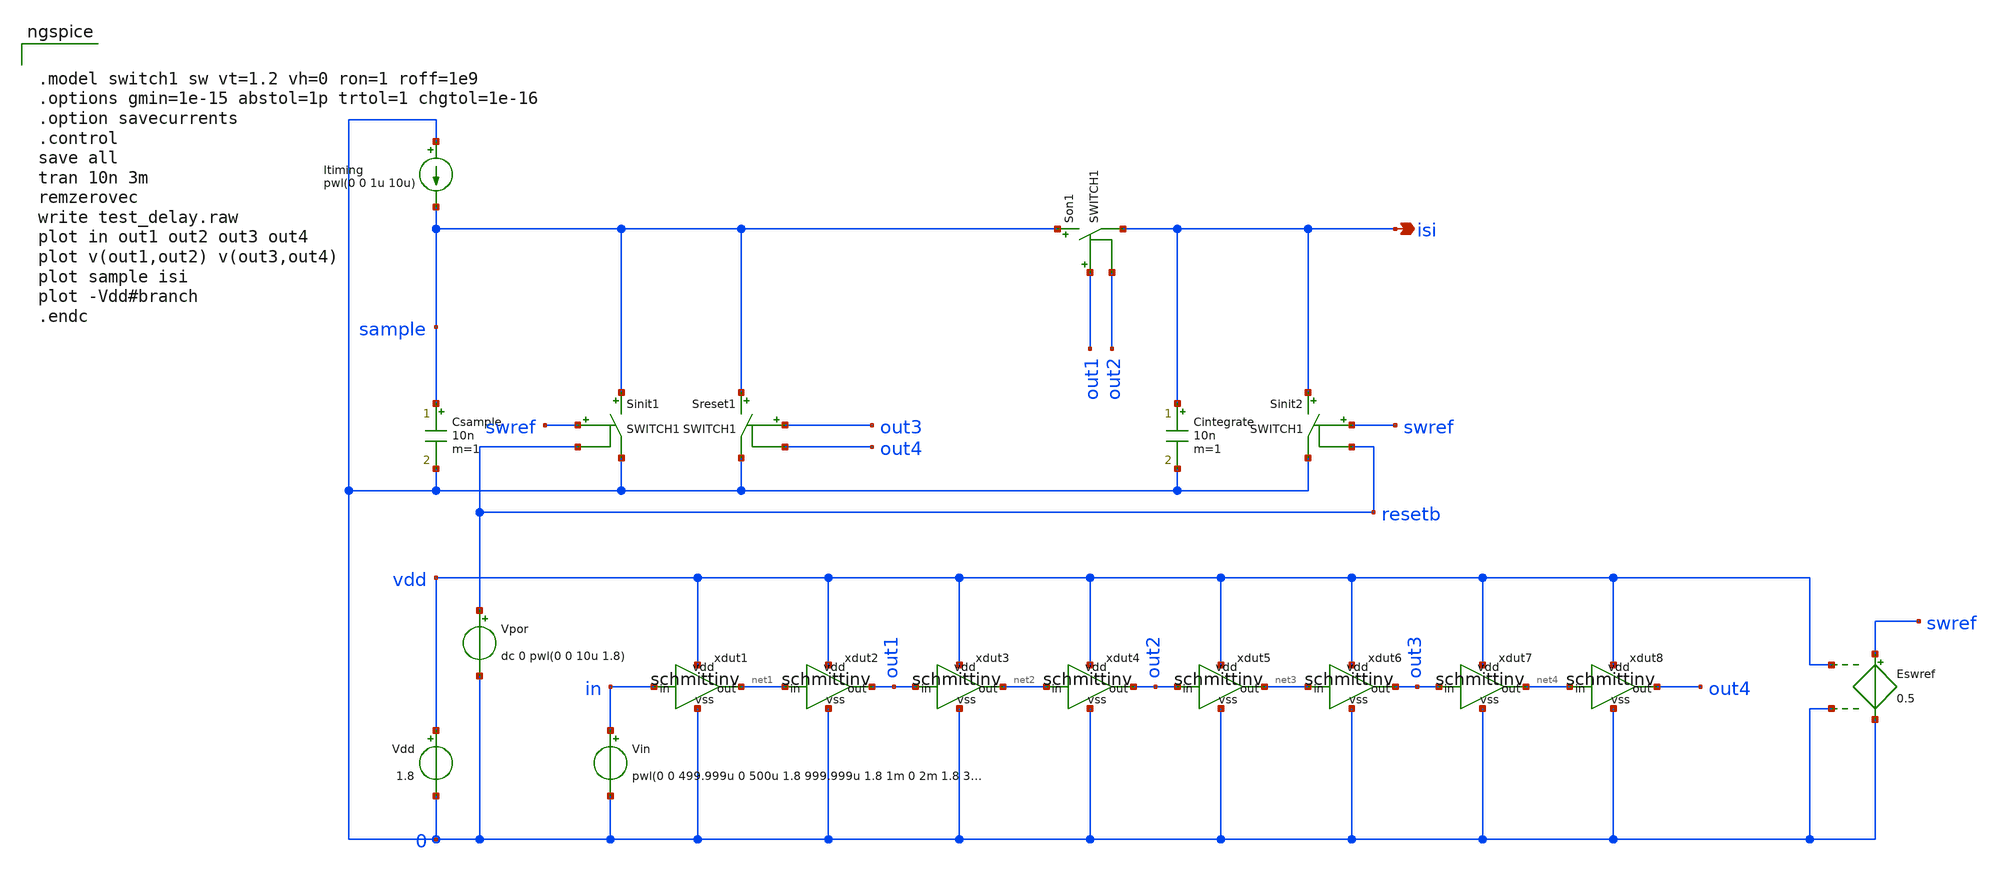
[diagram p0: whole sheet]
** sch_path: xschem/test_delay.sch
* Copyright 2020 Stefan Frederik Schippers
* Licensed under the Apache License, Version 2.0 (the "License");
* you may not use this file except in compliance with the License.
* You may obtain a copy of the License at
* https://www.apache.org/licenses/LICENSE-2.0
* Unless required by applicable law or agreed to in writing, software
* distributed under the License is distributed on an "AS IS" BASIS,
* WITHOUT WARRANTIES OR CONDITIONS OF ANY KIND, either express or implied.
* See the License for the specific language governing permissions and
* limitations under the License.
**.subckt test_delay isi
*.opin isi
Vdd vdd 0 1.8
xdut1 vdd in net1 0 schmittinv
Vin in 0 pwl(0 0 499.999u 0 500u 1.8 999.999u 1.8 1m 0 2m 1.8 3m 0)
xdut2 vdd net1 out1 0 schmittinv
xdut3 vdd out1 net2 0 schmittinv
xdut4 vdd net2 out2 0 schmittinv
Csample sample 0 10n m=1
Itiming 0 sample pwl(0 0 1u 10u)
Cintegrate isi 0 10n m=1
Sreset1 sample 0 out3 out4 SWITCH1
Eswref swref 0 vdd 0 0.5
Son1 sample isi out1 out2 SWITCH1
Sinit1 sample 0 swref resetb SWITCH1
Sinit2 isi 0 swref resetb SWITCH1
Vpor resetb 0 dc 0 pwl(0 0 10u 1.8)
xdut5 vdd out2 net3 0 schmittinv
xdut6 vdd net3 out3 0 schmittinv
xdut7 vdd out3 net4 0 schmittinv
xdut8 vdd net4 out4 0 schmittinv
**** begin user architecture code


.model switch1 sw vt=1.2 vh=0 ron=1 roff=1e9
.options gmin=1e-15 abstol=1p trtol=1 chgtol=1e-16
.option savecurrents
.control
save all
tran 10n 3m
remzerovec
write test_delay.raw
plot in out1 out2 out3 out4
plot v(out1,out2) v(out3,out4)
plot sample isi
plot -Vdd#branch
.endc


 .lib $::SKYWATER_MODELS/sky130.lib.spice tt

.param mc_mm_switch=0
.param mc_pr_switch=1


**** end user architecture code
**.ends

* expanding   symbol:  schmittinv.sym # of pins=4
** sym_path: schmittinv.sym
** sch_path: schmittinv.sch
.subckt schmittinv vdd in out vss
*.iopin vdd
*.iopin vss
*.ipin in
*.opin out
XM1 dn in vss vss sky130_fd_pr__nfet_01v8 L=8 W=0.5 nf=1 ad='int((1 + 1)/2) * 0.5 / 1 * 0.29' as='int((1 + 2)/2) * 0.5 / 1 * 0.29'
+ pd='2*int((1 + 1)/2) * (0.5 / 1 + 0.29)' ps='2*int((1 + 2)/2) * (0.5 / 1 + 0.29)' nrd='0.29 / 0.5 ' nrs='0.29 / 0.5 '
+ sa=0 sb=0 sd=0 mult=1 m=1
XM5 dp in vdd vdd sky130_fd_pr__pfet_01v8 L=2 W=0.5 nf=1 ad='int((nf+1)/2) * W/nf * 0.29' as='int((nf+2)/2) * W/nf * 0.29'
+ pd='2*int((nf+1)/2) * (W/nf + 0.29)' ps='2*int((nf+2)/2) * (W/nf + 0.29)' nrd='0.29 / W' nrs='0.29 / W'
+ sa=0 sb=0 sd=0 mult=1 m=1
XM3 vdd out dsn vss sky130_fd_pr__nfet_01v8 L=12 W=0.5 nf=1 ad='int((1 + 1)/2) * 0.5 / 1 * 0.29' as='int((1 + 2)/2) * 0.5 / 1 * 0.29'
+ pd='2*int((1 + 1)/2) * (0.5 / 1 + 0.29)' ps='2*int((1 + 2)/2) * (0.5 / 1 + 0.29)' nrd='0.29 / 0.5 ' nrs='0.29 / 0.5 '
+ sa=0 sb=0 sd=0 mult=1 m=1
XM6 vss out dp vdd sky130_fd_pr__pfet_01v8 L=4 W=0.5 nf=1 ad='int((nf+1)/2) * W/nf * 0.29' as='int((nf+2)/2) * W/nf * 0.29'
+ pd='2*int((nf+1)/2) * (W/nf + 0.29)' ps='2*int((nf+2)/2) * (W/nf + 0.29)' nrd='0.29 / W' nrs='0.29 / W'
+ sa=0 sb=0 sd=0 mult=1 m=1
XM4 out in dp vdd sky130_fd_pr__pfet_01v8 L=2 W=0.5 nf=1 ad='int((nf+1)/2) * W/nf * 0.29' as='int((nf+2)/2) * W/nf * 0.29'
+ pd='2*int((nf+1)/2) * (W/nf + 0.29)' ps='2*int((nf+2)/2) * (W/nf + 0.29)' nrd='0.29 / W' nrs='0.29 / W'
+ sa=0 sb=0 sd=0 mult=1 m=1
XM2 out in dn vss sky130_fd_pr__nfet_01v8 L=8 W=0.5 nf=1 ad='int((1 + 1)/2) * 0.5 / 1 * 0.29' as='int((1 + 2)/2) * 0.5 / 1 * 0.29'
+ pd='2*int((1 + 1)/2) * (0.5 / 1 + 0.29)' ps='2*int((1 + 2)/2) * (0.5 / 1 + 0.29)' nrd='0.29 / 0.5 ' nrs='0.29 / 0.5 '
+ sa=0 sb=0 sd=0 mult=1 m=1
XM30 dsn out dn vss sky130_fd_pr__nfet_01v8 L=12 W=0.5 nf=1 ad='int((1 + 1)/2) * 0.5 / 1 * 0.29' as='int((1 + 2)/2) * 0.5 / 1 * 0.29'
+ pd='2*int((1 + 1)/2) * (0.5 / 1 + 0.29)' ps='2*int((1 + 2)/2) * (0.5 / 1 + 0.29)' nrd='0.29 / 0.5 ' nrs='0.29 / 0.5 '
+ sa=0 sb=0 sd=0 mult=1 m=1
.ends

.end
